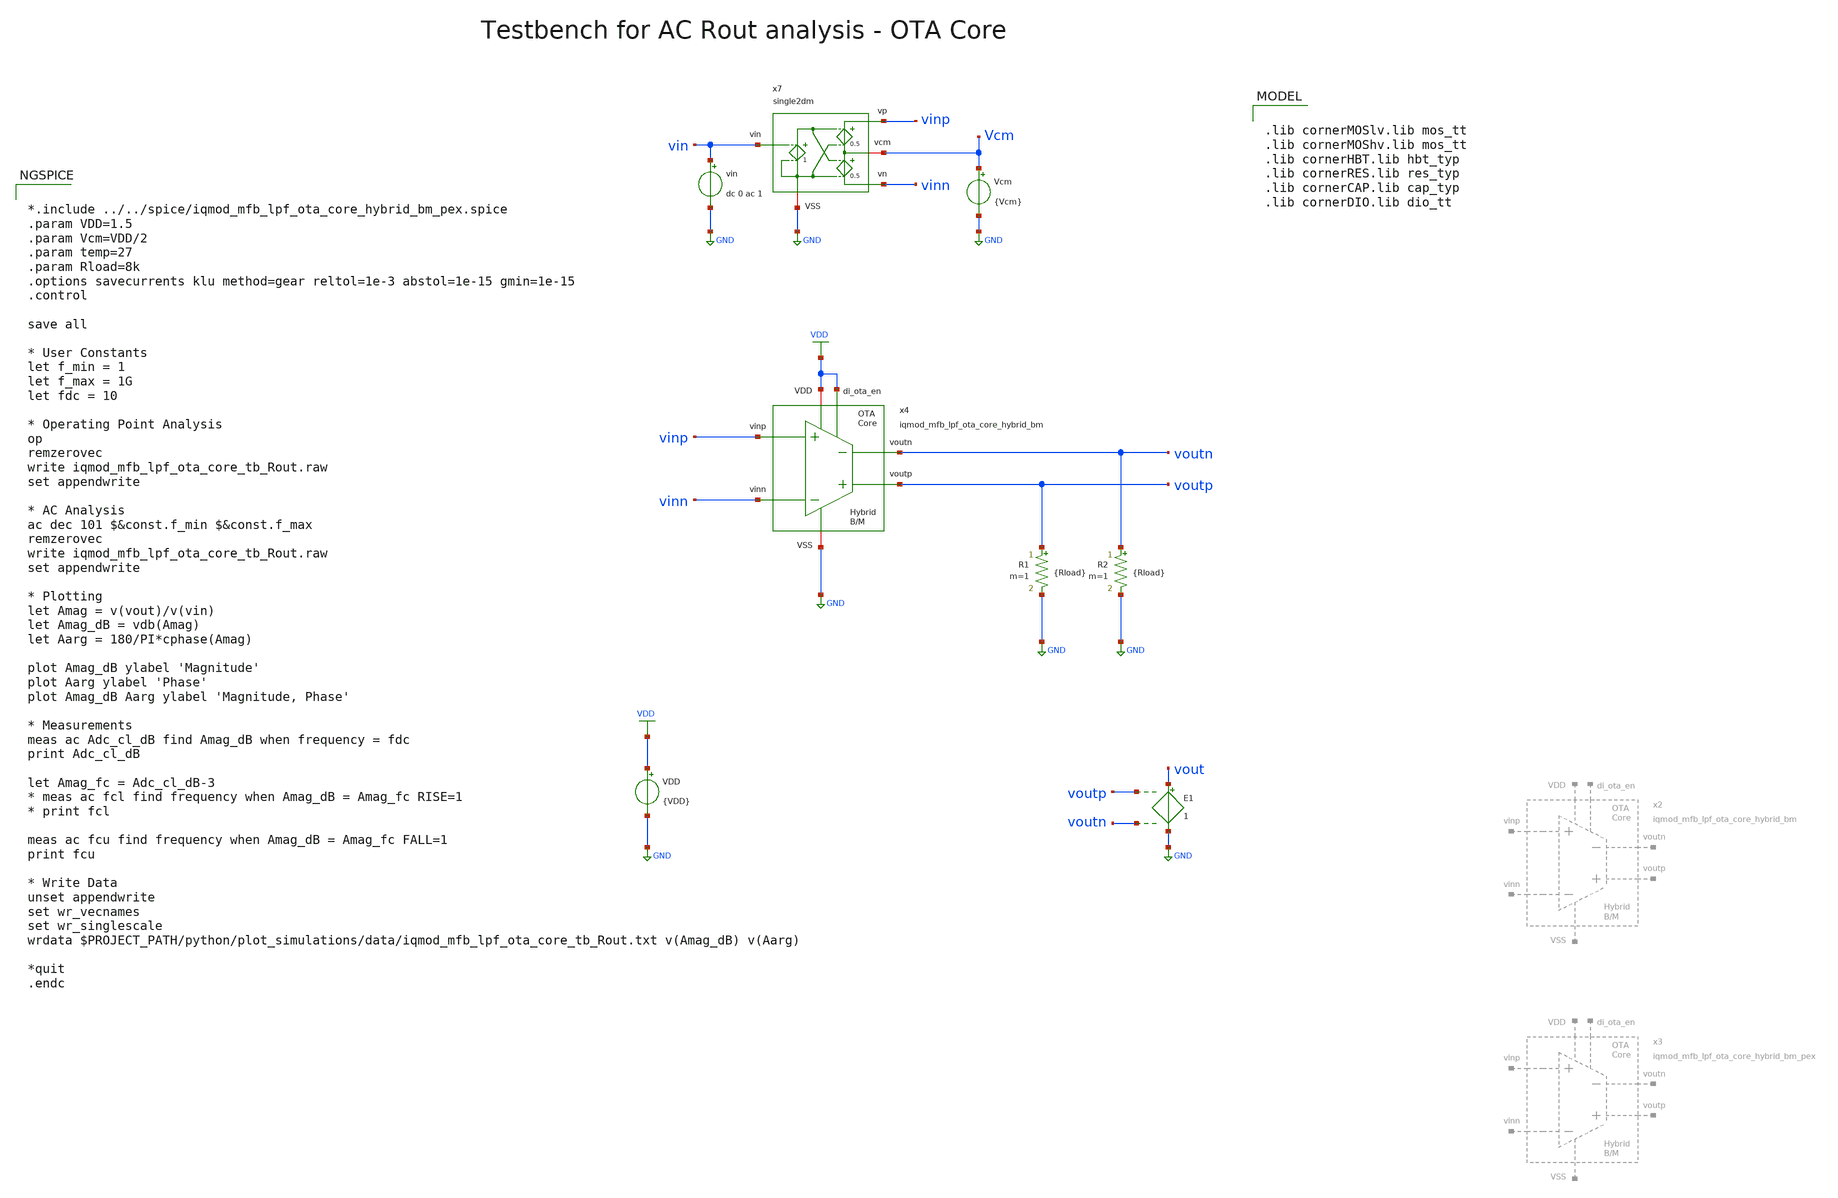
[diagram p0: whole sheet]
** sch_path: ihp130/macros/iqmod/xschem/testbenches/iqmod_mfb_lpf_ota_core_tb_Rout.sch
**.subckt iqmod_mfb_lpf_ota_core_tb_Rout
VDD VDD GND {VDD}
E1 vout GND voutp voutn 1
R1 voutp GND {Rload} m=1
R2 voutn GND {Rload} m=1
x4 voutp voutn vinn vinp VDD GND VDD iqmod_mfb_lpf_ota_core_hybrid_bm
Vcm Vcm GND {Vcm}
vin vin GND dc 0 ac 1
x7 vinp vin Vcm GND vinn single2dm
**** begin user architecture code


*.include ../../spice/iqmod_mfb_lpf_ota_core_hybrid_bm_pex.spice
.param VDD=1.5
.param Vcm=VDD/2
.param temp=27
.param Rload=8k
.options savecurrents klu method=gear reltol=1e-3 abstol=1e-15 gmin=1e-15
.control

save all

* User Constants
let f_min = 1
let f_max = 1G
let fdc = 10

* Operating Point Analysis
op
remzerovec
write iqmod_mfb_lpf_ota_core_tb_Rout.raw
set appendwrite

* AC Analysis
ac dec 101 $&const.f_min $&const.f_max
remzerovec
write iqmod_mfb_lpf_ota_core_tb_Rout.raw
set appendwrite

* Plotting
let Amag = v(vout)/v(vin)
let Amag_dB = vdb(Amag)
let Aarg = 180/PI*cphase(Amag)

plot Amag_dB ylabel 'Magnitude'
plot Aarg ylabel 'Phase'
plot Amag_dB Aarg ylabel 'Magnitude, Phase'

* Measurements
meas ac Adc_cl_dB find Amag_dB when frequency = fdc
print Adc_cl_dB

let Amag_fc = Adc_cl_dB-3
* meas ac fcl find frequency when Amag_dB = Amag_fc RISE=1
* print fcl

meas ac fcu find frequency when Amag_dB = Amag_fc FALL=1
print fcu

* Write Data
unset appendwrite
set wr_vecnames
set wr_singlescale
wrdata $PROJECT_PATH/python/plot_simulations/data/iqmod_mfb_lpf_ota_core_tb_Rout.txt v(Amag_dB)
+ v(Aarg)

*quit
.endc



.lib cornerMOSlv.lib mos_tt
.lib cornerMOShv.lib mos_tt
.lib cornerHBT.lib hbt_typ
.lib cornerRES.lib res_typ
.lib cornerCAP.lib cap_typ
.lib cornerDIO.lib dio_tt

**** end user architecture code
**.ends
.GLOBAL GND
.GLOBAL VDD
.end
